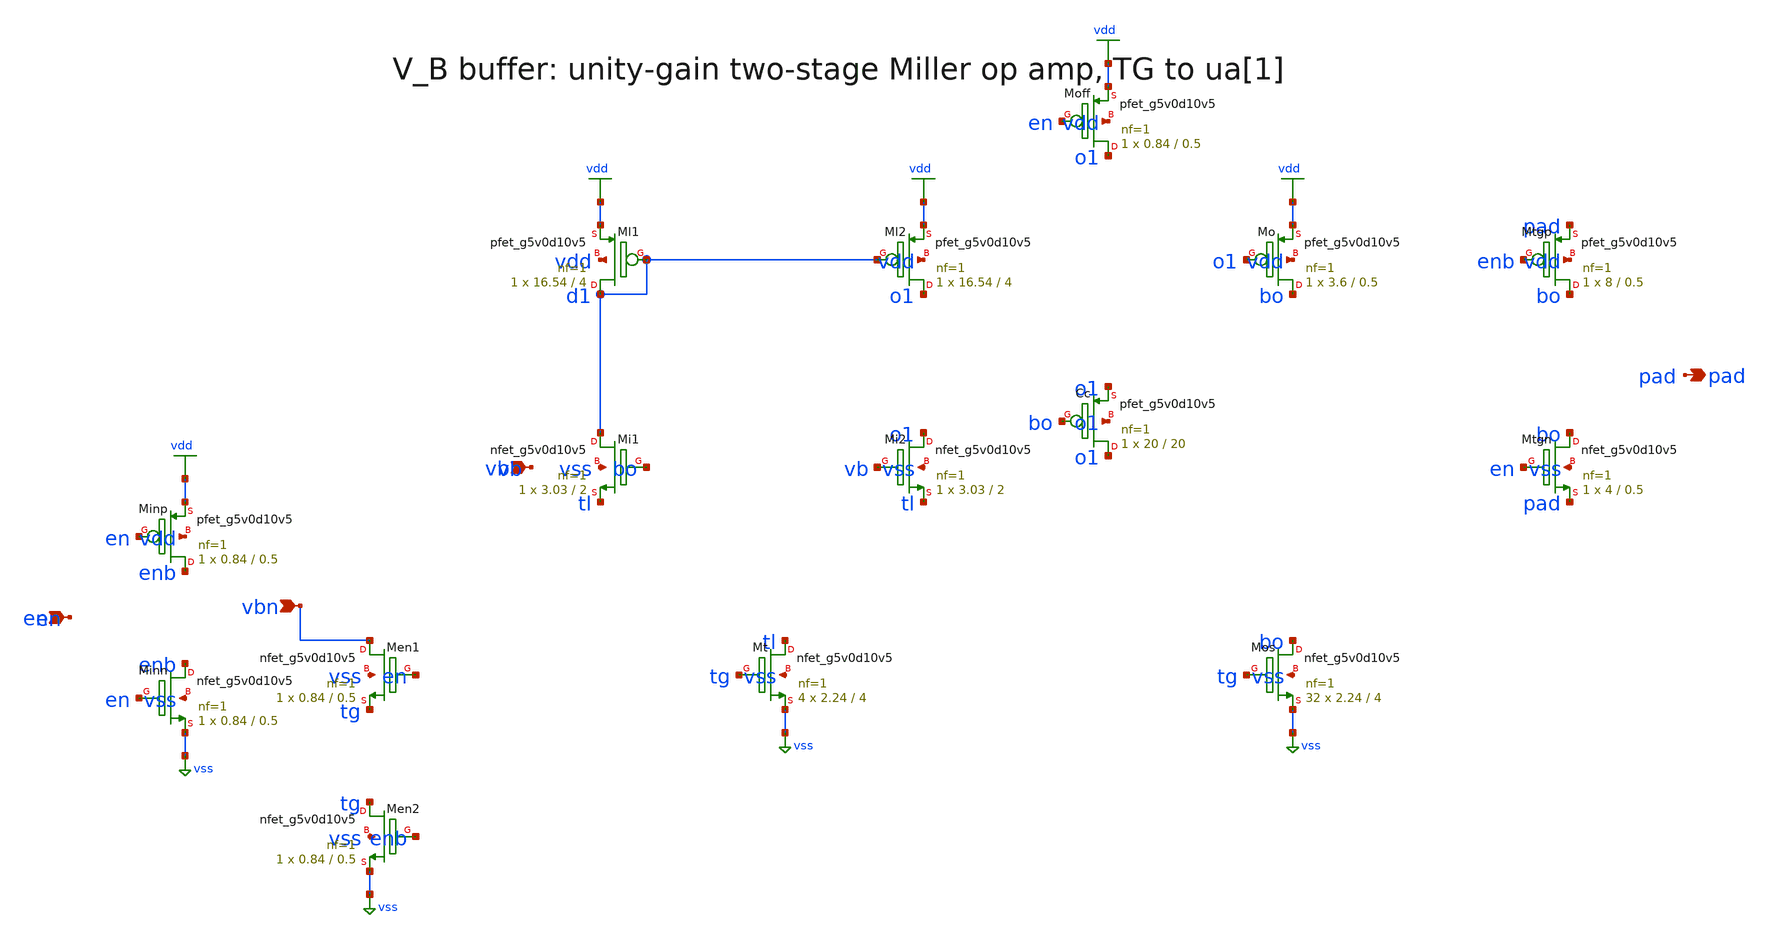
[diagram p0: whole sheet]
** sch_path: xschem/rt5w_vbbuf.sch
**.subckt rt5w_vbbuf vb vbn en pad
*.ipin vb
*.ipin vbn
*.ipin en
*.opin pad
XMl1 d1 d1 vdd vdd sky130_fd_pr__pfet_g5v0d10v5 L=4 W=16.54 nf=1 ad=4.797 as=4.797 pd=33.66 ps=33.66
+ nrd=0.01753 nrs=0.01753 sa=0 sb=0 sd=0 mult=1 m=1
XMl2 o1 d1 vdd vdd sky130_fd_pr__pfet_g5v0d10v5 L=4 W=16.54 nf=1 ad=4.797 as=4.797 pd=33.66 ps=33.66
+ nrd=0.01753 nrs=0.01753 sa=0 sb=0 sd=0 mult=1 m=1
XMi1 d1 bo tl vss sky130_fd_pr__nfet_g5v0d10v5 L=2 W=3.03 nf=1 ad=0.8787 as=0.8787 pd=6.64 ps=6.64
+ nrd=0.09571 nrs=0.09571 sa=0 sb=0 sd=0 mult=1 m=1
XMi2 o1 vb tl vss sky130_fd_pr__nfet_g5v0d10v5 L=2 W=3.03 nf=1 ad=0.8787 as=0.8787 pd=6.64 ps=6.64
+ nrd=0.09571 nrs=0.09571 sa=0 sb=0 sd=0 mult=1 m=1
XMt tl tg vss vss sky130_fd_pr__nfet_g5v0d10v5 L=4 W=2.24 nf=1 ad=0.6496 as=0.6496 pd=5.06 ps=5.06
+ nrd=0.1295 nrs=0.1295 sa=0 sb=0 sd=0 mult=4 m=4
XMo bo o1 vdd vdd sky130_fd_pr__pfet_g5v0d10v5 L=0.5 W=3.6 nf=1 ad=1.044 as=1.044 pd=7.78 ps=7.78
+ nrd=0.08056 nrs=0.08056 sa=0 sb=0 sd=0 mult=1 m=1
XMos bo tg vss vss sky130_fd_pr__nfet_g5v0d10v5 L=4 W=2.24 nf=1 ad=0.6496 as=0.6496 pd=5.06 ps=5.06
+ nrd=0.1295 nrs=0.1295 sa=0 sb=0 sd=0 mult=32 m=32
XCc o1 bo o1 o1 sky130_fd_pr__pfet_g5v0d10v5 L=20 W=20 nf=1 ad=5.8 as=5.8 pd=40.58 ps=40.58
+ nrd=0.0145 nrs=0.0145 sa=0 sb=0 sd=0 mult=1 m=1
XMoff o1 en vdd vdd sky130_fd_pr__pfet_g5v0d10v5 L=0.5 W=0.84 nf=1 ad=0.2436 as=0.2436 pd=2.26
+ ps=2.26 nrd=0.3452 nrs=0.3452 sa=0 sb=0 sd=0 mult=1 m=1
XMen1 vbn en tg vss sky130_fd_pr__nfet_g5v0d10v5 L=0.5 W=0.84 nf=1 ad=0.2436 as=0.2436 pd=2.26
+ ps=2.26 nrd=0.3452 nrs=0.3452 sa=0 sb=0 sd=0 mult=1 m=1
XMen2 tg enb vss vss sky130_fd_pr__nfet_g5v0d10v5 L=0.5 W=0.84 nf=1 ad=0.2436 as=0.2436 pd=2.26
+ ps=2.26 nrd=0.3452 nrs=0.3452 sa=0 sb=0 sd=0 mult=1 m=1
XMinp enb en vdd vdd sky130_fd_pr__pfet_g5v0d10v5 L=0.5 W=0.84 nf=1 ad=0.2436 as=0.2436 pd=2.26
+ ps=2.26 nrd=0.3452 nrs=0.3452 sa=0 sb=0 sd=0 mult=1 m=1
XMinn enb en vss vss sky130_fd_pr__nfet_g5v0d10v5 L=0.5 W=0.84 nf=1 ad=0.2436 as=0.2436 pd=2.26
+ ps=2.26 nrd=0.3452 nrs=0.3452 sa=0 sb=0 sd=0 mult=1 m=1
XMtgn bo en pad vss sky130_fd_pr__nfet_g5v0d10v5 L=0.5 W=4 nf=1 ad=1.16 as=1.16 pd=8.58 ps=8.58
+ nrd=0.0725 nrs=0.0725 sa=0 sb=0 sd=0 mult=1 m=1
XMtgp bo enb pad vdd sky130_fd_pr__pfet_g5v0d10v5 L=0.5 W=8 nf=1 ad=2.32 as=2.32 pd=16.58 ps=16.58
+ nrd=0.03625 nrs=0.03625 sa=0 sb=0 sd=0 mult=1 m=1
**.ends
.GLOBAL vdd
.GLOBAL vss
.end
